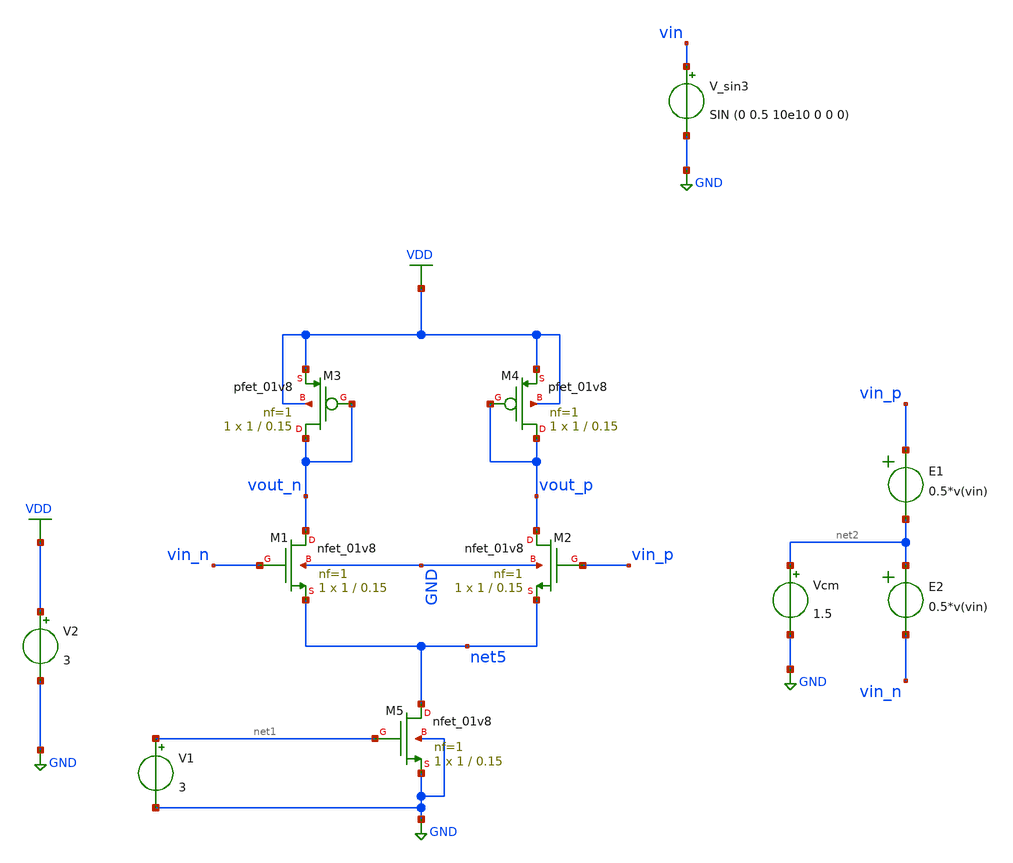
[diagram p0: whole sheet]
** sch_path: schem/amp.sch
**.subckt amp
XM2 vout_p vin_p net5 GND sky130_fd_pr__nfet_01v8 L=0.15 W=1 nf=1 ad='int((1 + 1)/2) * 1 / 1 * 0.29'
+ as='int((1 + 2)/2) * 1 / 1 * 0.29' pd='2*int((1 + 1)/2) * (1 / 1 + 0.29)' ps='2*int((1 + 2)/2) * (1 / 1 + 0.29)'
+ nrd='0.29 / 1 ' nrs='0.29 / 1 ' sa=0 sb=0 sd=0 mult=1 m=1
XM3 vout_n vout_n VDD VDD sky130_fd_pr__pfet_01v8 L=0.15 W=1 nf=1 ad='int((1 + 1)/2) * 1 / 1 * 0.29'
+ as='int((1 + 2)/2) * 1 / 1 * 0.29' pd='2*int((1 + 1)/2) * (1 / 1 + 0.29)' ps='2*int((1 + 2)/2) * (1 / 1 + 0.29)'
+ nrd='0.29 / 1 ' nrs='0.29 / 1 ' sa=0 sb=0 sd=0 mult=1 m=1
XM1 vout_n vin_n net5 GND sky130_fd_pr__nfet_01v8 L=0.15 W=1 nf=1 ad='int((1 + 1)/2) * 1 / 1 * 0.29'
+ as='int((1 + 2)/2) * 1 / 1 * 0.29' pd='2*int((1 + 1)/2) * (1 / 1 + 0.29)' ps='2*int((1 + 2)/2) * (1 / 1 + 0.29)'
+ nrd='0.29 / 1 ' nrs='0.29 / 1 ' sa=0 sb=0 sd=0 mult=1 m=1
XM4 vout_p vout_p VDD VDD sky130_fd_pr__pfet_01v8 L=0.15 W=1 nf=1 ad='int((1 + 1)/2) * 1 / 1 * 0.29'
+ as='int((1 + 2)/2) * 1 / 1 * 0.29' pd='2*int((1 + 1)/2) * (1 / 1 + 0.29)' ps='2*int((1 + 2)/2) * (1 / 1 + 0.29)'
+ nrd='0.29 / 1 ' nrs='0.29 / 1 ' sa=0 sb=0 sd=0 mult=1 m=1
XM5 net5 net1 GND GND sky130_fd_pr__nfet_01v8 L=0.15 W=1 nf=1 ad='int((1 + 1)/2) * 1 / 1 * 0.29' as='int((1 + 2)/2) * 1 / 1 * 0.29'
+ pd='2*int((1 + 1)/2) * (1 / 1 + 0.29)' ps='2*int((1 + 2)/2) * (1 / 1 + 0.29)' nrd='0.29 / 1 ' nrs='0.29 / 1 '
+ sa=0 sb=0 sd=0 mult=1 m=1
V1 net1 GND 3
Vcm net2 GND 1.5
V2 VDD GND 3
V_sin3 vin GND SIN (0 0.5 10e10 0 0 0)
E1 vin_p net2 VOL=' 0.5*v(vin) '
E2 net2 vin_n VOL=' 0.5*v(vin) '
**** begin user architecture code

.control
    save all
    +v(vin) v(vin_p) v(vin_n) v(vout_p) v(vout_n) v(net5)
    +@m.xm1.msky130_fd_pr__nfet_01v8[id] @m.xm1.msky130_fd_pr__nfet_01v8[gm]
    +@m.xm2.msky130_fd_pr__nfet_01v8[id] @m.xm2.msky130_fd_pr__nfet_01v8[gm]
    +@m.xm3.msky130_fd_pr__pfet_01v8[id] @m.xm3.msky130_fd_pr__pfet_01v8[gm]
    +@m.xm4.msky130_fd_pr__pfet_01v8[id] @m.xm4.msky130_fd_pr__pfet_01v8[gm]
    +@m.xm5.msky130_fd_pr__nfet_01v8[id] @m.xm5.msky130_fd_pr__nfet_01v8[gm]
    op
    write op.raw
    tran 1p 10n
    save all v(vi_i) v(vi_p) v(vi_n)
    write tran.raw
.endc



** opencircuitdesign pdks install
.lib $::SKYWATER_MODELS/sky130.lib.spice tt

**** end user architecture code
**.ends
.GLOBAL VDD
.GLOBAL GND
.end
